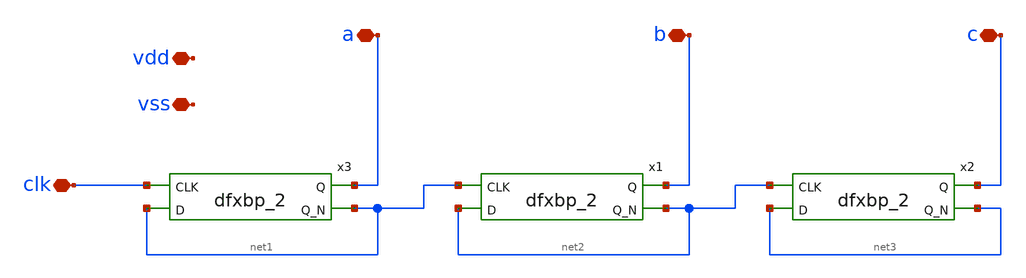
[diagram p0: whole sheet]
** sch_path: xschem/divider/divider.sch
**.subckt divider clk vdd vss a b c
*.iopin clk
*.iopin vdd
*.iopin vss
*.iopin a
*.iopin b
*.iopin c
x3 clk net1 VSS VSS VDD VDD a net1 sky130_fd_sc_hd__dfxbp_2
x1 net1 net2 VSS VSS VDD VDD b net2 sky130_fd_sc_hd__dfxbp_2
x2 net2 net3 VSS VSS VDD VDD c net3 sky130_fd_sc_hd__dfxbp_2
**.ends
.end
